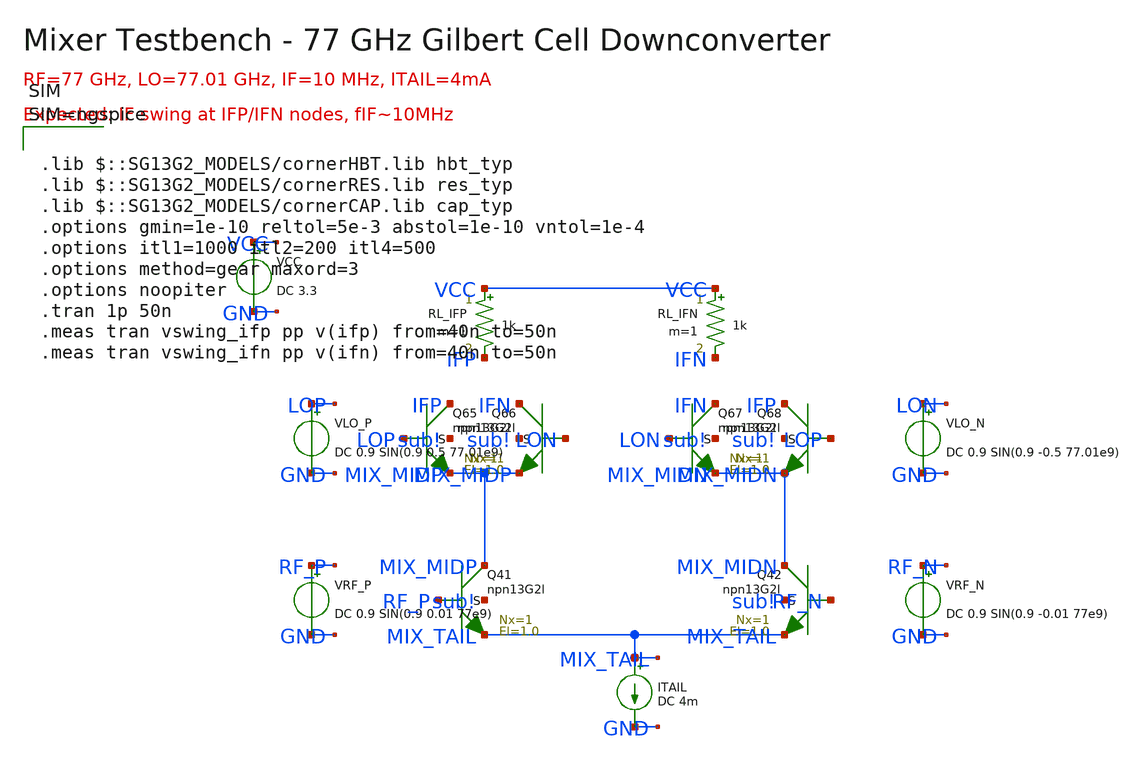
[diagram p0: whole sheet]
** sch_path: layout/testbenches/tb_mixer.sch
**.subckt tb_mixer
XQ41 MIX_MIDP RF_P MIX_TAIL sub! npn13G2l Nx=1 El=1.0 mm_ok=1
XQ42 MIX_MIDN RF_N MIX_TAIL sub! npn13G2l Nx=1 El=1.0 mm_ok=1
XQ65 IFP LOP MIX_MIDP sub! npn13G2l Nx=1 El=1.0 mm_ok=1
XQ66 IFN LON MIX_MIDP sub! npn13G2l Nx=1 El=1.0 mm_ok=1
XQ67 IFN LON MIX_MIDN sub! npn13G2l Nx=1 El=1.0 mm_ok=1
XQ68 IFP LOP MIX_MIDN sub! npn13G2l Nx=1 El=1.0 mm_ok=1
RL_IFP VCC IFP 1k m=1
RL_IFN VCC IFN 1k m=1
VCC VCC GND DC 3.3
ITAIL MIX_TAIL GND DC 4m
VRF_P RF_P GND DC 0.9 SIN(0.9 0.01 77e9)
VRF_N RF_N GND DC 0.9 SIN(0.9 -0.01 77e9)
VLO_P LOP GND DC 0.9 SIN(0.9 0.5 77.01e9)
VLO_N LON GND DC 0.9 SIN(0.9 -0.5 77.01e9)
**** begin user architecture code



.lib $::SG13G2_MODELS/cornerHBT.lib hbt_typ
.lib $::SG13G2_MODELS/cornerRES.lib res_typ
.lib $::SG13G2_MODELS/cornerCAP.lib cap_typ
.options gmin=1e-10 reltol=5e-3 abstol=1e-10 vntol=1e-4
.options itl1=1000 itl2=200 itl4=500
.options method=gear maxord=3
.options noopiter
.tran 1p 50n
.meas tran vswing_ifp pp v(ifp) from=40n to=50n
.meas tran vswing_ifn pp v(ifn) from=40n to=50n



**** end user architecture code
**.ends
.end
